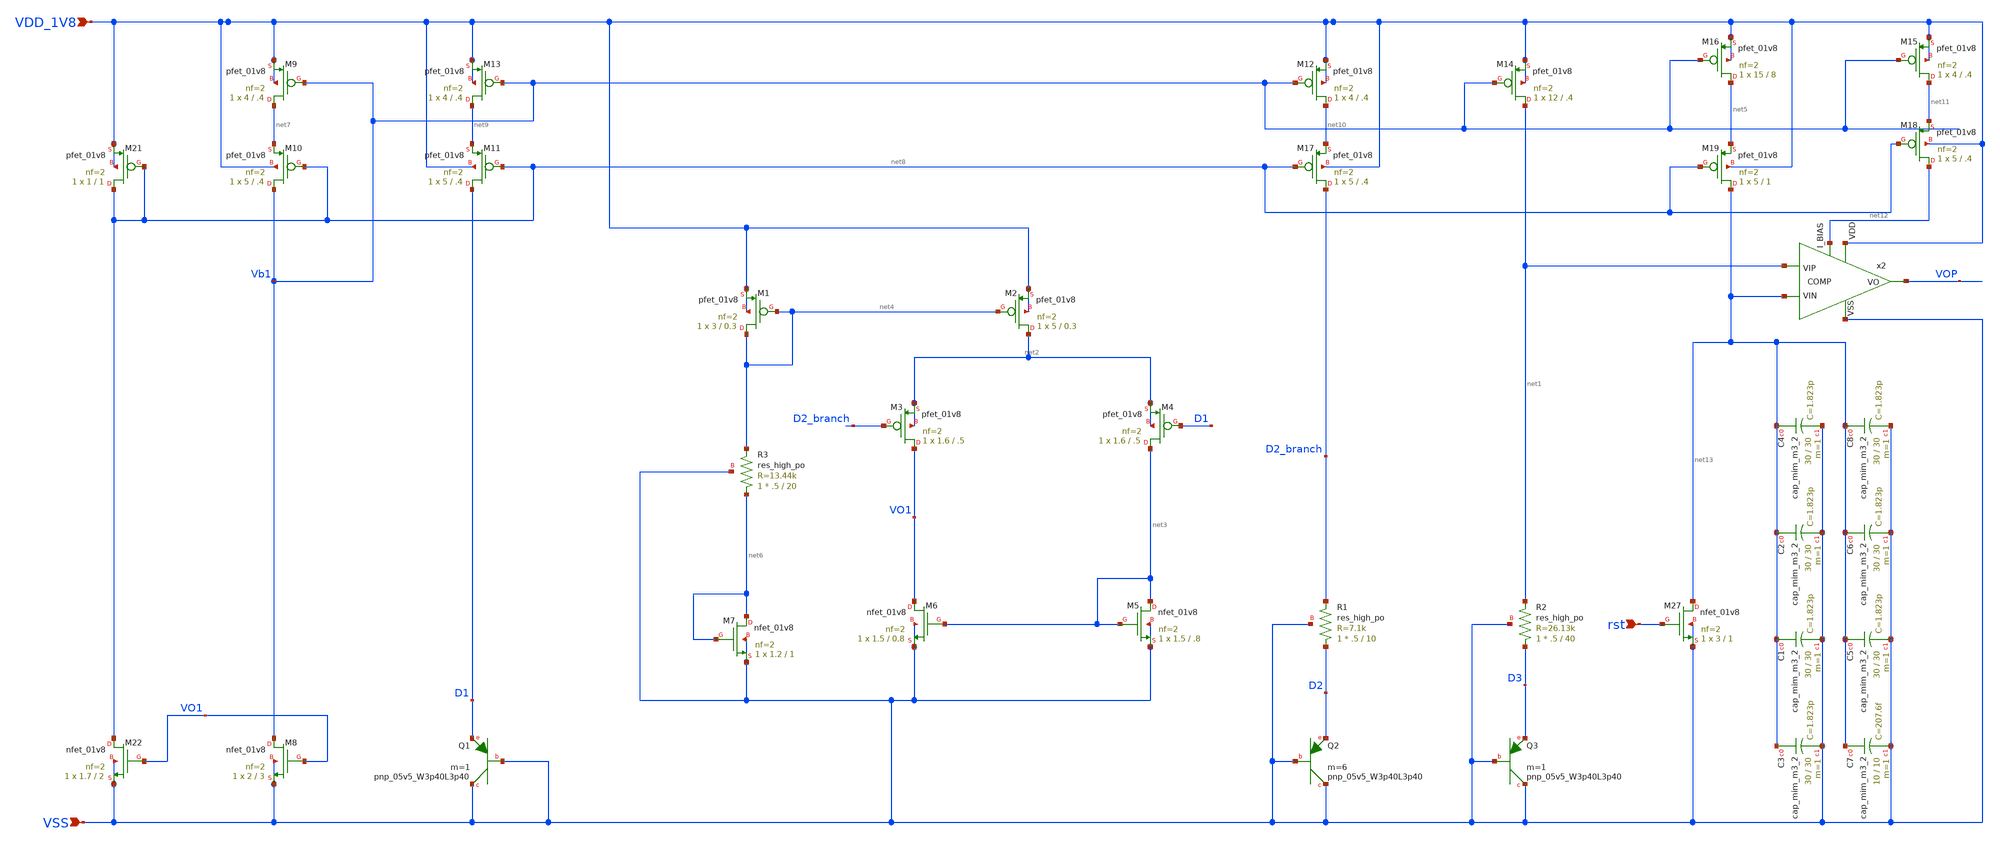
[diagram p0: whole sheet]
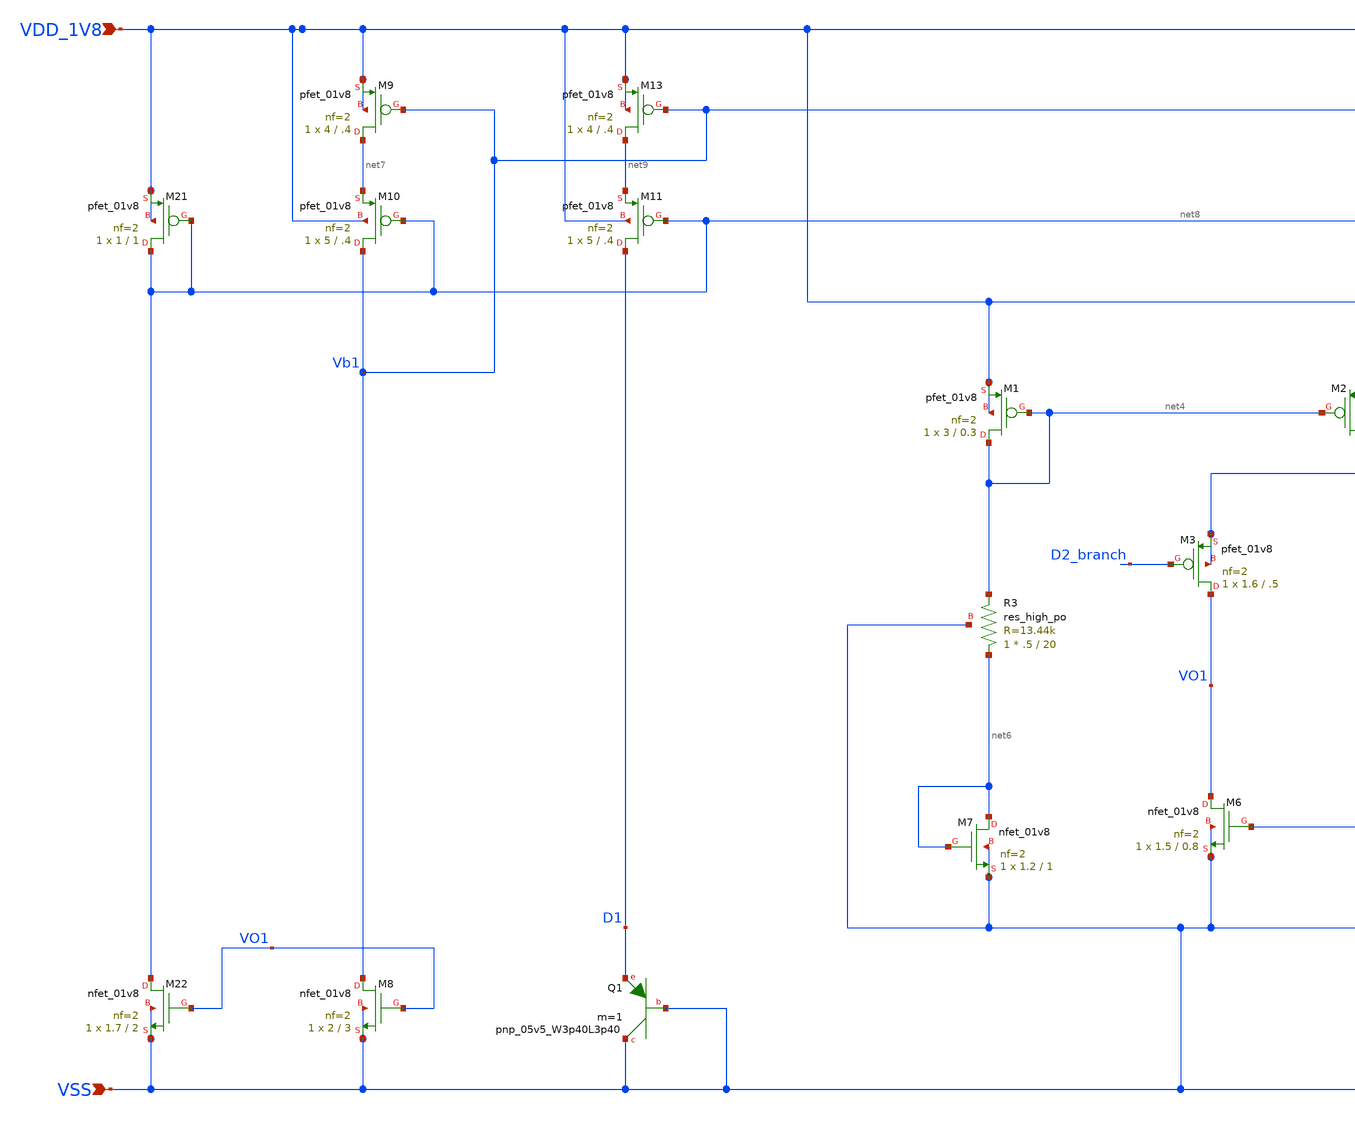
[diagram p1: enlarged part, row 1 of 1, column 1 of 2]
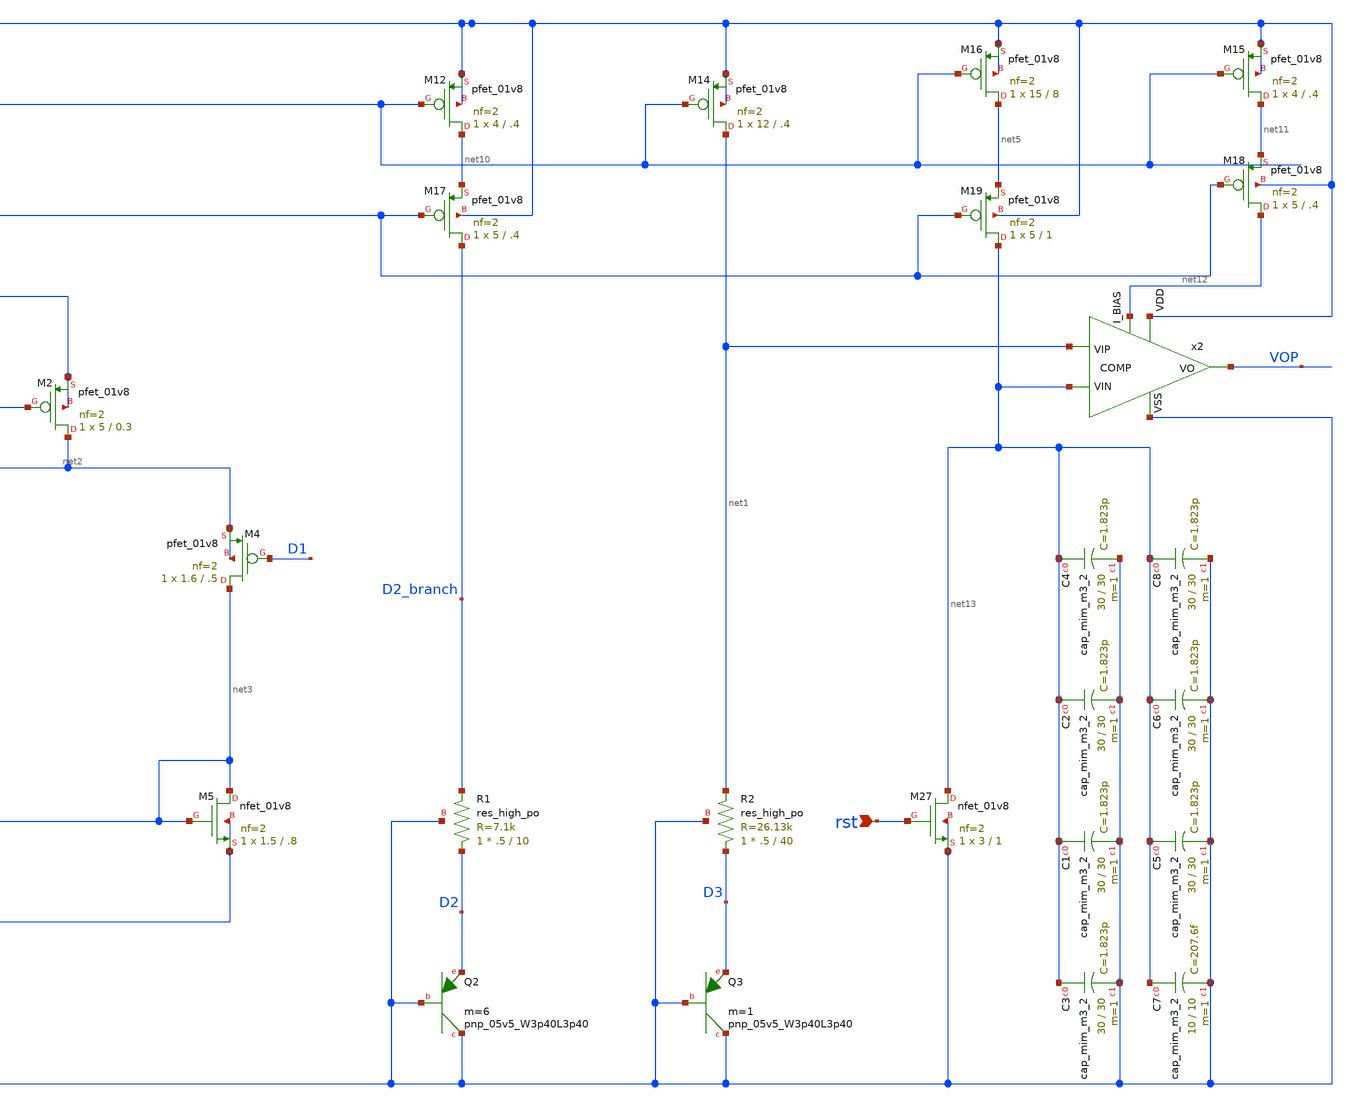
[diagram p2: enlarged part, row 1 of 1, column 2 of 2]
** sch_path: design/CNR_GR02_SKY130NM/CNR_GR02.sch
**.subckt CNR_GR02 VDD_1V8 VSS rst
*.ipin VDD_1V8
*.ipin VSS
*.ipin rst
x2 VDD_1V8 net1 net13 VOP net12 VSS COMP
XQ2 VSS VSS D2 sky130_fd_pr__pnp_05v5_W3p40L3p40 m=6
XQ1 VSS VSS D1 sky130_fd_pr__pnp_05v5_W3p40L3p40 m=1
XM12 net10 Vb1 VDD_1V8 VDD_1V8 sky130_fd_pr__pfet_01v8 L=.4 W=4 nf=2 ad='int((nf+1)/2) * W/nf * 0.29'
+ as='int((nf+2)/2) * W/nf * 0.29' pd='2*int((nf+1)/2) * (W/nf + 0.29)' ps='2*int((nf+2)/2) * (W/nf + 0.29)'
+ nrd='0.29 / W' nrs='0.29 / W' sa=0 sb=0 sd=0 mult=1 m=1
XM13 net9 Vb1 VDD_1V8 VDD_1V8 sky130_fd_pr__pfet_01v8 L=.4 W=4 nf=2 ad='int((nf+1)/2) * W/nf * 0.29'
+ as='int((nf+2)/2) * W/nf * 0.29' pd='2*int((nf+1)/2) * (W/nf + 0.29)' ps='2*int((nf+2)/2) * (W/nf + 0.29)'
+ nrd='0.29 / W' nrs='0.29 / W' sa=0 sb=0 sd=0 mult=1 m=1
XM14 net1 Vb1 VDD_1V8 VDD_1V8 sky130_fd_pr__pfet_01v8 L=.4 W=12 nf=2 ad='int((nf+1)/2) * W/nf * 0.29'
+ as='int((nf+2)/2) * W/nf * 0.29' pd='2*int((nf+1)/2) * (W/nf + 0.29)' ps='2*int((nf+2)/2) * (W/nf + 0.29)'
+ nrd='0.29 / W' nrs='0.29 / W' sa=0 sb=0 sd=0 mult=1 m=1
XQ3 VSS VSS D3 sky130_fd_pr__pnp_05v5_W3p40L3p40 m=1
XM16 net5 Vb1 VDD_1V8 VDD_1V8 sky130_fd_pr__pfet_01v8 L=8 W=15 nf=2 ad='int((nf+1)/2) * W/nf * 0.29'
+ as='int((nf+2)/2) * W/nf * 0.29' pd='2*int((nf+1)/2) * (W/nf + 0.29)' ps='2*int((nf+2)/2) * (W/nf + 0.29)'
+ nrd='0.29 / W' nrs='0.29 / W' sa=0 sb=0 sd=0 mult=1 m=1
XM1 net4 net4 VDD_1V8 VDD_1V8 sky130_fd_pr__pfet_01v8 L=0.3 W=3 nf=2 ad='int((nf+1)/2) * W/nf * 0.29'
+ as='int((nf+2)/2) * W/nf * 0.29' pd='2*int((nf+1)/2) * (W/nf + 0.29)' ps='2*int((nf+2)/2) * (W/nf + 0.29)'
+ nrd='0.29 / W' nrs='0.29 / W' sa=0 sb=0 sd=0 mult=1 m=1
XM2 net2 net4 VDD_1V8 VDD_1V8 sky130_fd_pr__pfet_01v8 L=0.3 W=5 nf=2 ad='int((nf+1)/2) * W/nf * 0.29'
+ as='int((nf+2)/2) * W/nf * 0.29' pd='2*int((nf+1)/2) * (W/nf + 0.29)' ps='2*int((nf+2)/2) * (W/nf + 0.29)'
+ nrd='0.29 / W' nrs='0.29 / W' sa=0 sb=0 sd=0 mult=1 m=1
XM3 VO1 D2_branch net2 net2 sky130_fd_pr__pfet_01v8 L=.5 W=1.6 nf=2 ad='int((nf+1)/2) * W/nf * 0.29'
+ as='int((nf+2)/2) * W/nf * 0.29' pd='2*int((nf+1)/2) * (W/nf + 0.29)' ps='2*int((nf+2)/2) * (W/nf + 0.29)'
+ nrd='0.29 / W' nrs='0.29 / W' sa=0 sb=0 sd=0 mult=1 m=1
XM4 net3 D1 net2 net2 sky130_fd_pr__pfet_01v8 L=.5 W=1.6 nf=2 ad='int((nf+1)/2) * W/nf * 0.29' as='int((nf+2)/2) * W/nf * 0.29'
+ pd='2*int((nf+1)/2) * (W/nf + 0.29)' ps='2*int((nf+2)/2) * (W/nf + 0.29)' nrd='0.29 / W' nrs='0.29 / W'
+ sa=0 sb=0 sd=0 mult=1 m=1
XM5 net3 net3 VSS VSS sky130_fd_pr__nfet_01v8 L=.8 W=1.5 nf=2 ad='int((nf+1)/2) * W/nf * 0.29' as='int((nf+2)/2) * W/nf * 0.29'
+ pd='2*int((nf+1)/2) * (W/nf + 0.29)' ps='2*int((nf+2)/2) * (W/nf + 0.29)' nrd='0.29 / W' nrs='0.29 / W'
+ sa=0 sb=0 sd=0 mult=1 m=1
XM6 VO1 net3 VSS VSS sky130_fd_pr__nfet_01v8 L=0.8 W=1.5 nf=2 ad='int((nf+1)/2) * W/nf * 0.29' as='int((nf+2)/2) * W/nf * 0.29'
+ pd='2*int((nf+1)/2) * (W/nf + 0.29)' ps='2*int((nf+2)/2) * (W/nf + 0.29)' nrd='0.29 / W' nrs='0.29 / W'
+ sa=0 sb=0 sd=0 mult=1 m=1
XR2 D3 net1 VSS sky130_fd_pr__res_high_po W=.5 L=40 mult=1 m=1
XR1 D2 D2_branch VSS sky130_fd_pr__res_high_po W=.5 L=10 mult=1 m=1
XM7 net6 net6 VSS VSS sky130_fd_pr__nfet_01v8 L=1 W=1.2 nf=2 ad='int((nf+1)/2) * W/nf * 0.29' as='int((nf+2)/2) * W/nf * 0.29'
+ pd='2*int((nf+1)/2) * (W/nf + 0.29)' ps='2*int((nf+2)/2) * (W/nf + 0.29)' nrd='0.29 / W' nrs='0.29 / W'
+ sa=0 sb=0 sd=0 mult=1 m=1
XR3 net6 net4 VSS sky130_fd_pr__res_high_po W=.5 L=20 mult=1 m=1
XM8 Vb1 VO1 VSS VSS sky130_fd_pr__nfet_01v8 L=3 W=2 nf=2 ad='int((nf+1)/2) * W/nf * 0.29' as='int((nf+2)/2) * W/nf * 0.29'
+ pd='2*int((nf+1)/2) * (W/nf + 0.29)' ps='2*int((nf+2)/2) * (W/nf + 0.29)' nrd='0.29 / W' nrs='0.29 / W'
+ sa=0 sb=0 sd=0 mult=1 m=1
XM9 net7 Vb1 VDD_1V8 VDD_1V8 sky130_fd_pr__pfet_01v8 L=.4 W=4 nf=2 ad='int((nf+1)/2) * W/nf * 0.29' as='int((nf+2)/2) * W/nf * 0.29'
+ pd='2*int((nf+1)/2) * (W/nf + 0.29)' ps='2*int((nf+2)/2) * (W/nf + 0.29)' nrd='0.29 / W' nrs='0.29 / W'
+ sa=0 sb=0 sd=0 mult=1 m=1
XM10 Vb1 net8 net7 VDD_1V8 sky130_fd_pr__pfet_01v8 L=.4 W=5 nf=2 ad='int((nf+1)/2) * W/nf * 0.29' as='int((nf+2)/2) * W/nf * 0.29'
+ pd='2*int((nf+1)/2) * (W/nf + 0.29)' ps='2*int((nf+2)/2) * (W/nf + 0.29)' nrd='0.29 / W' nrs='0.29 / W'
+ sa=0 sb=0 sd=0 mult=1 m=1
XM11 D1 net8 net9 VDD_1V8 sky130_fd_pr__pfet_01v8 L=.4 W=5 nf=2 ad='int((nf+1)/2) * W/nf * 0.29' as='int((nf+2)/2) * W/nf * 0.29'
+ pd='2*int((nf+1)/2) * (W/nf + 0.29)' ps='2*int((nf+2)/2) * (W/nf + 0.29)' nrd='0.29 / W' nrs='0.29 / W'
+ sa=0 sb=0 sd=0 mult=1 m=1
XM17 D2_branch net8 net10 VDD_1V8 sky130_fd_pr__pfet_01v8 L=.4 W=5 nf=2 ad='int((nf+1)/2) * W/nf * 0.29'
+ as='int((nf+2)/2) * W/nf * 0.29' pd='2*int((nf+1)/2) * (W/nf + 0.29)' ps='2*int((nf+2)/2) * (W/nf + 0.29)'
+ nrd='0.29 / W' nrs='0.29 / W' sa=0 sb=0 sd=0 mult=1 m=1
XM21 net8 net8 VDD_1V8 VDD_1V8 sky130_fd_pr__pfet_01v8 L=1 W=1 nf=2 ad='int((nf+1)/2) * W/nf * 0.29'
+ as='int((nf+2)/2) * W/nf * 0.29' pd='2*int((nf+1)/2) * (W/nf + 0.29)' ps='2*int((nf+2)/2) * (W/nf + 0.29)'
+ nrd='0.29 / W' nrs='0.29 / W' sa=0 sb=0 sd=0 mult=1 m=1
XM22 net8 VO1 VSS VSS sky130_fd_pr__nfet_01v8 L=2 W=1.7 nf=2 ad='int((nf+1)/2) * W/nf * 0.29' as='int((nf+2)/2) * W/nf * 0.29'
+ pd='2*int((nf+1)/2) * (W/nf + 0.29)' ps='2*int((nf+2)/2) * (W/nf + 0.29)' nrd='0.29 / W' nrs='0.29 / W'
+ sa=0 sb=0 sd=0 mult=1 m=1
XM27 net13 rst VSS VSS sky130_fd_pr__nfet_01v8 L=1 W=3 nf=2 ad='int((nf+1)/2) * W/nf * 0.29' as='int((nf+2)/2) * W/nf * 0.29'
+ pd='2*int((nf+1)/2) * (W/nf + 0.29)' ps='2*int((nf+2)/2) * (W/nf + 0.29)' nrd='0.29 / W' nrs='0.29 / W'
+ sa=0 sb=0 sd=0 mult=1 m=1
XM15 net11 Vb1 VDD_1V8 VDD_1V8 sky130_fd_pr__pfet_01v8 L=.4 W=4 nf=2 ad='int((nf+1)/2) * W/nf * 0.29'
+ as='int((nf+2)/2) * W/nf * 0.29' pd='2*int((nf+1)/2) * (W/nf + 0.29)' ps='2*int((nf+2)/2) * (W/nf + 0.29)'
+ nrd='0.29 / W' nrs='0.29 / W' sa=0 sb=0 sd=0 mult=1 m=1
XM18 net12 net8 net11 VDD_1V8 sky130_fd_pr__pfet_01v8 L=.4 W=5 nf=2 ad='int((nf+1)/2) * W/nf * 0.29'
+ as='int((nf+2)/2) * W/nf * 0.29' pd='2*int((nf+1)/2) * (W/nf + 0.29)' ps='2*int((nf+2)/2) * (W/nf + 0.29)'
+ nrd='0.29 / W' nrs='0.29 / W' sa=0 sb=0 sd=0 mult=1 m=1
XM19 net13 net8 net5 VDD_1V8 sky130_fd_pr__pfet_01v8 L=1 W=5 nf=2 ad='int((nf+1)/2) * W/nf * 0.29' as='int((nf+2)/2) * W/nf * 0.29'
+ pd='2*int((nf+1)/2) * (W/nf + 0.29)' ps='2*int((nf+2)/2) * (W/nf + 0.29)' nrd='0.29 / W' nrs='0.29 / W'
+ sa=0 sb=0 sd=0 mult=1 m=1
XC1 net13 VSS sky130_fd_pr__cap_mim_m3_2 W=30 L=30 MF=1 m=1
XC2 net13 VSS sky130_fd_pr__cap_mim_m3_2 W=30 L=30 MF=1 m=1
XC3 net13 VSS sky130_fd_pr__cap_mim_m3_2 W=30 L=30 MF=1 m=1
XC4 net13 VSS sky130_fd_pr__cap_mim_m3_2 W=30 L=30 MF=1 m=1
XC5 net13 VSS sky130_fd_pr__cap_mim_m3_2 W=30 L=30 MF=1 m=1
XC6 net13 VSS sky130_fd_pr__cap_mim_m3_2 W=30 L=30 MF=1 m=1
XC7 net13 VSS sky130_fd_pr__cap_mim_m3_2 W=10 L=10 MF=1 m=1
XC8 net13 VSS sky130_fd_pr__cap_mim_m3_2 W=30 L=30 MF=1 m=1
**.ends
.end
